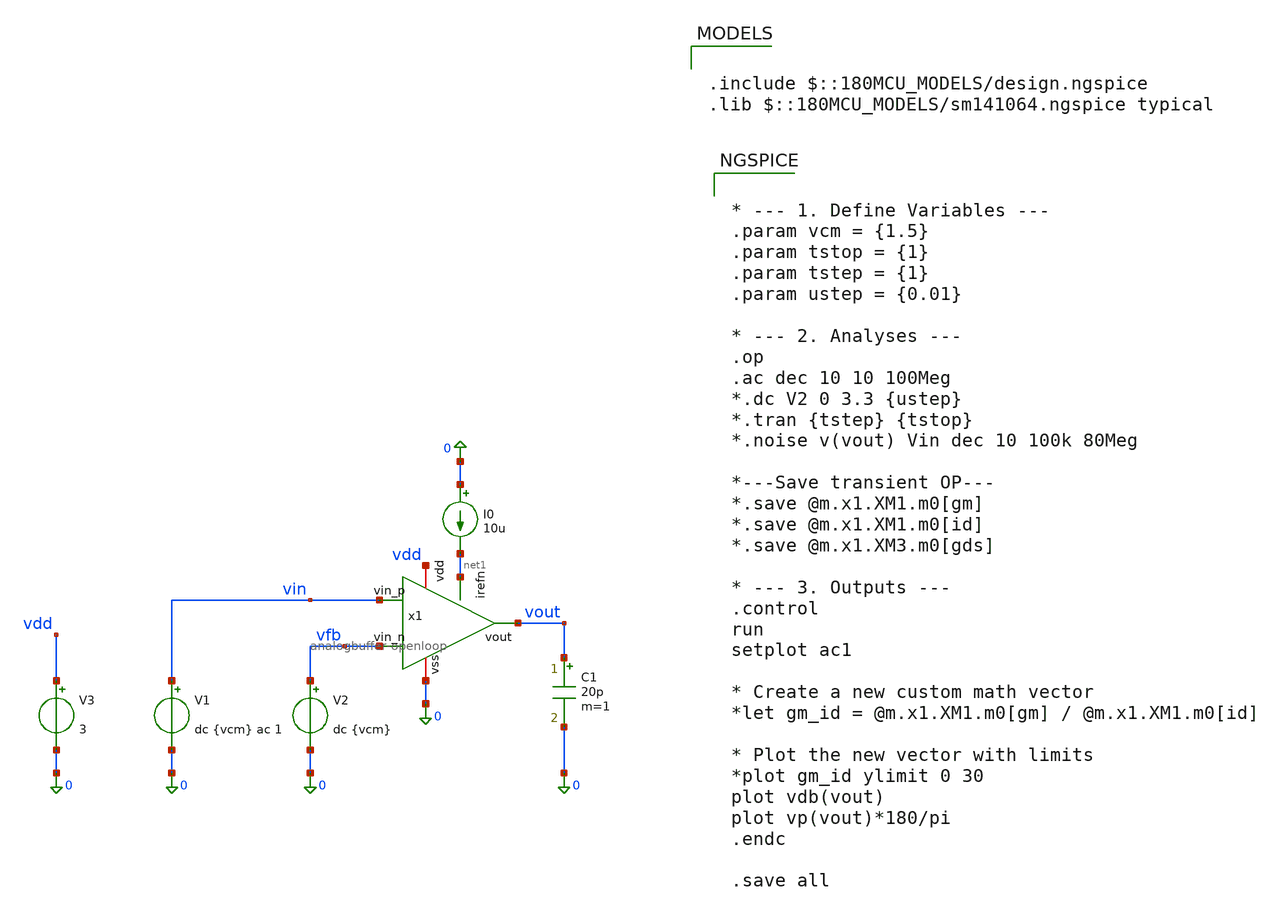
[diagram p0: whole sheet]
** sch_path: Tobias/2026 07 14 Intermediate Results/analogbuffer/analogbuffer-openloop-tb.sch
**.subckt analogbuffer-openloop-tb
x1 vdd net1 vin vout vfb 0 analogbuffer-openloop
V1 vin 0 dc {vcm} ac 1
V2 vfb 0 dc {vcm}
C1 vout 0 20p m=1
I0 0 net1 10u
V3 vdd 0 3
**** begin user architecture code


* --- 1. Define Variables ---
.param vcm = {1.5}
.param tstop = {1}
.param tstep = {1}
.param ustep = {0.01}

* --- 2. Analyses ---
.op
.ac dec 10 10 100Meg
*.dc V2 0 3.3 {ustep}
*.tran {tstep} {tstop}
*.noise v(vout) Vin dec 10 100k 80Meg

*---Save transient OP---
*.save @m.x1.XM1.m0[gm]
*.save @m.x1.XM1.m0[id]
*.save @m.x1.XM3.m0[gds]

* --- 3. Outputs ---
.control
run
setplot ac1

* Create a new custom math vector
*let gm_id = @m.x1.XM1.m0[gm] / @m.x1.XM1.m0[id]

* Plot the new vector with limits
*plot gm_id ylimit 0 30
plot vdb(vout)
plot vp(vout)*180/pi
.endc

.save all



.include $::180MCU_MODELS/design.ngspice
.lib $::180MCU_MODELS/sm141064.ngspice typical

**** end user architecture code
**.ends
.end
